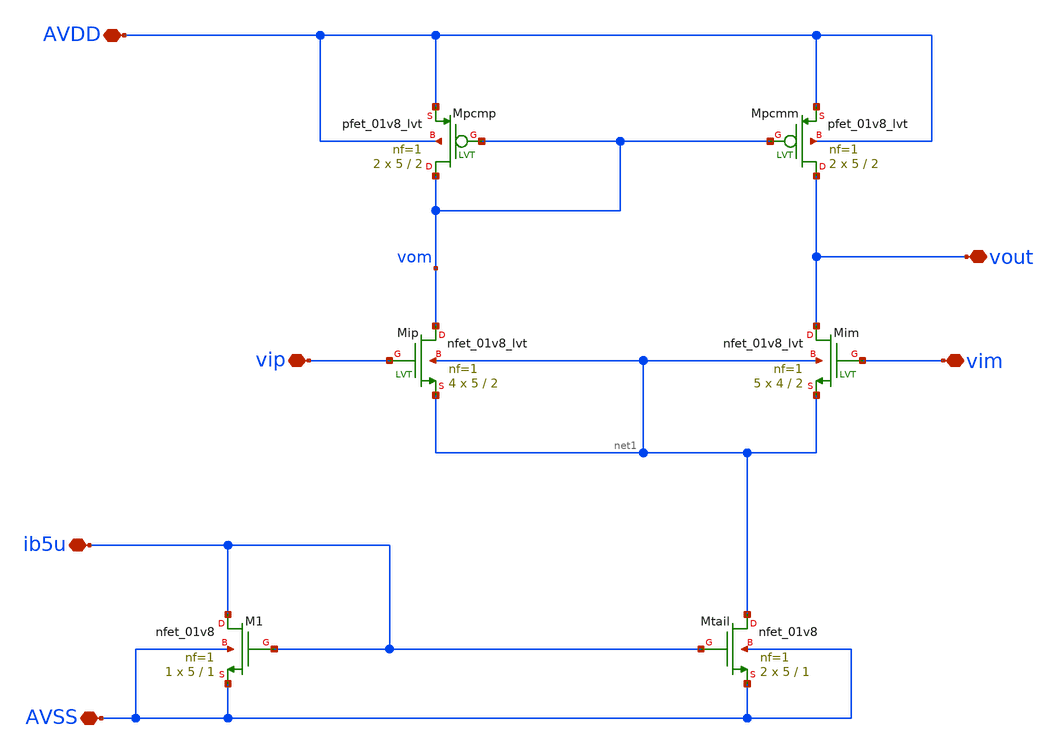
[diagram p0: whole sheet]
** sch_path: xschem/xschem/opamp_nmos.sch
**.subckt opamp_nmos vip vim vout ib5u AVDD AVSS
*.iopin vip
*.iopin vim
*.iopin vout
*.iopin ib5u
*.iopin AVDD
*.iopin AVSS
XM1 ib5u ib5u AVSS AVSS sky130_fd_pr__nfet_01v8 L=1 W=5 nf=1 ad='int((1 + 1)/2) * 5 / 1 * 0.29' as='int((1 + 2)/2) * 5 / 1 * 0.29'
+ pd='2*int((1 + 1)/2) * (5 / 1 + 0.29)' ps='2*int((1 + 2)/2) * (5 / 1 + 0.29)' nrd='0.29 / 5 ' nrs='0.29 / 5 '
+ sa=0 sb=0 sd=0 mult=1 m=1
XMtail net1 ib5u AVSS AVSS sky130_fd_pr__nfet_01v8 L=1 W=5 nf=1 ad='int((1 + 1)/2) * 5 / 1 * 0.29' as='int((1 + 2)/2) * 5 / 1 * 0.29'
+ pd='2*int((1 + 1)/2) * (5 / 1 + 0.29)' ps='2*int((1 + 2)/2) * (5 / 1 + 0.29)' nrd='0.29 / 5 ' nrs='0.29 / 5 '
+ sa=0 sb=0 sd=0 mult=2 m=2
XMip vom vip net1 net1 sky130_fd_pr__nfet_01v8_lvt L=2 W=5 nf=1 ad='int((1 + 1)/2) * 5 / 1 * 0.29' as='int((1 + 2)/2) * 5 / 1 * 0.29'
+ pd='2*int((1 + 1)/2) * (5 / 1 + 0.29)' ps='2*int((1 + 2)/2) * (5 / 1 + 0.29)' nrd='0.29 / 5 ' nrs='0.29 / 5 '
+ sa=0 sb=0 sd=0 mult=4 m=4
XMim vout vim net1 net1 sky130_fd_pr__nfet_01v8_lvt L=2 W=4 nf=1 ad='int((1 + 1)/2) * 4 / 1 * 0.29' as='int((1 + 2)/2) * 4 / 1 * 0.29'
+ pd='2*int((1 + 1)/2) * (4 / 1 + 0.29)' ps='2*int((1 + 2)/2) * (4 / 1 + 0.29)' nrd='0.29 / 4 ' nrs='0.29 / 4 '
+ sa=0 sb=0 sd=0 mult=5 m=5
XMpcmp vom vom AVDD AVDD sky130_fd_pr__pfet_01v8_lvt L=2 W=5 nf=1 ad='int((1 + 1)/2) * 5 / 1 * 0.29'
+ as='int((1 + 2)/2) * 5 / 1 * 0.29' pd='2*int((1 + 1)/2) * (5 / 1 + 0.29)' ps='2*int((1 + 2)/2) * (5 / 1 + 0.29)'
+ nrd='0.29 / 5 ' nrs='0.29 / 5 ' sa=0 sb=0 sd=0 mult=2 m=2
XMpcmm vout vom AVDD AVDD sky130_fd_pr__pfet_01v8_lvt L=2 W=5 nf=1 ad='int((1 + 1)/2) * 5 / 1 * 0.29'
+ as='int((1 + 2)/2) * 5 / 1 * 0.29' pd='2*int((1 + 1)/2) * (5 / 1 + 0.29)' ps='2*int((1 + 2)/2) * (5 / 1 + 0.29)'
+ nrd='0.29 / 5 ' nrs='0.29 / 5 ' sa=0 sb=0 sd=0 mult=2 m=2
**.ends
.end
